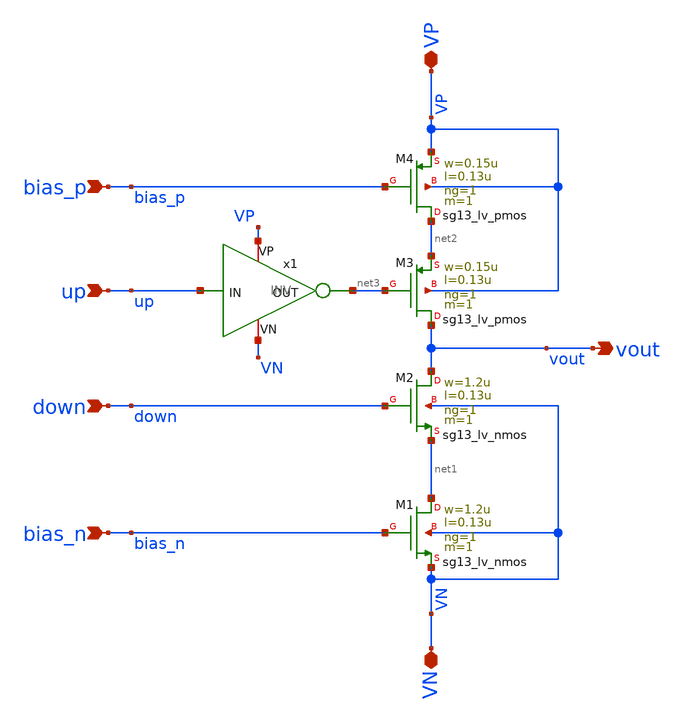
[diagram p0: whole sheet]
** sch_path: 30_MHz_Fractional_N_PLL/design_data/xschem/CHRG_PUMP.sch
**.subckt CHRG_PUMP bias_p up down bias_n VN VP vout
*.ipin bias_p
*.ipin up
*.ipin down
*.ipin bias_n
*.iopin VN
*.iopin VP
*.opin vout
XM1 net1 bias_n VN VN sg13_lv_nmos w=1.2u l=0.13u ng=1 m=1 mm_ok=1
XM2 vout down net1 VN sg13_lv_nmos w=1.2u l=0.13u ng=1 m=1 mm_ok=1
XM3 vout net3 net2 VP sg13_lv_pmos w=0.15u l=0.13u ng=1 m=1 mm_ok=1
XM4 net2 bias_p VP VP sg13_lv_pmos w=0.15u l=0.13u ng=1 m=1 mm_ok=1
x1 VP up net3 VN INV
**.ends

* expanding   symbol:  INV.sym # of pins=4
** sym_path: 30_MHz_Fractional_N_PLL/design_data/xschem/INV.sym
** sch_path: 30_MHz_Fractional_N_PLL/design_data/xschem/INV.sch
.subckt INV VP IN OUT VN
*.iopin VN
*.iopin VP
*.ipin IN
*.opin OUT
XM1 OUT IN VN VN sg13_lv_nmos w=0.15u l=0.13u ng=1 m=1 mm_ok=1
XM2 OUT IN VP VP sg13_lv_pmos w=0.3u l=0.13u ng=1 m=1 mm_ok=1
.ends

.end
